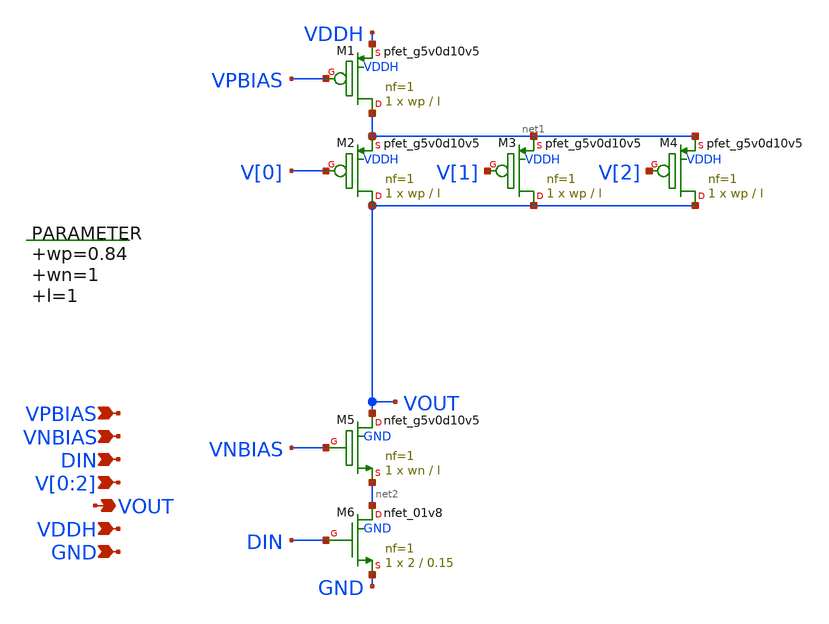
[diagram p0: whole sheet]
** sch_path: xschem/pd_network_parallel.sch
**.subckt pd_network_parallel VPBIAS VNBIAS DIN V[0],V[1],V[2] VOUT VDDH GND
*.ipin VPBIAS
*.ipin VNBIAS
*.ipin DIN
*.ipin V[0],V[1],V[2]
*.opin VOUT
*.ipin VDDH
*.ipin GND
.param wp=0.84 wn=1 l=1

XM1 net1 VPBIAS VDDH VDDH sky130_fd_pr__pfet_g5v0d10v5 L=l W=wp nf=1 ad='int((nf+1)/2) * W/nf * 0.29'
+ as='int((nf+2)/2) * W/nf * 0.29' pd='2*int((nf+1)/2) * (W/nf + 0.29)' ps='2*int((nf+2)/2) * (W/nf + 0.29)'
+ nrd='0.29 / W' nrs='0.29 / W' sa=0 sb=0 sd=0 mult=1 m=1
XM5 VOUT VNBIAS net2 GND sky130_fd_pr__nfet_g5v0d10v5 L=l W=wn nf=1 ad='int((nf+1)/2) * W/nf * 0.29'
+ as='int((nf+2)/2) * W/nf * 0.29' pd='2*int((nf+1)/2) * (W/nf + 0.29)' ps='2*int((nf+2)/2) * (W/nf + 0.29)'
+ nrd='0.29 / W' nrs='0.29 / W' sa=0 sb=0 sd=0 mult=1 m=1
XM2 VOUT V[0] net1 VDDH sky130_fd_pr__pfet_g5v0d10v5 L=l W=wp nf=1 ad='int((nf+1)/2) * W/nf * 0.29' as='int((nf+2)/2) * W/nf * 0.29'
+ pd='2*int((nf+1)/2) * (W/nf + 0.29)' ps='2*int((nf+2)/2) * (W/nf + 0.29)' nrd='0.29 / W' nrs='0.29 / W'
+ sa=0 sb=0 sd=0 mult=1 m=1
XM3 VOUT V[1] net1 VDDH sky130_fd_pr__pfet_g5v0d10v5 L=l W=wp nf=1 ad='int((nf+1)/2) * W/nf * 0.29' as='int((nf+2)/2) * W/nf * 0.29'
+ pd='2*int((nf+1)/2) * (W/nf + 0.29)' ps='2*int((nf+2)/2) * (W/nf + 0.29)' nrd='0.29 / W' nrs='0.29 / W'
+ sa=0 sb=0 sd=0 mult=1 m=1
XM4 VOUT V[2] net1 VDDH sky130_fd_pr__pfet_g5v0d10v5 L=l W=wp nf=1 ad='int((nf+1)/2) * W/nf * 0.29' as='int((nf+2)/2) * W/nf * 0.29'
+ pd='2*int((nf+1)/2) * (W/nf + 0.29)' ps='2*int((nf+2)/2) * (W/nf + 0.29)' nrd='0.29 / W' nrs='0.29 / W'
+ sa=0 sb=0 sd=0 mult=1 m=1
XM6 net2 DIN GND GND sky130_fd_pr__nfet_01v8 L=0.15 W=2 nf=1 ad='int((nf+1)/2) * W/nf * 0.29' as='int((nf+2)/2) * W/nf * 0.29'
+ pd='2*int((nf+1)/2) * (W/nf + 0.29)' ps='2*int((nf+2)/2) * (W/nf + 0.29)' nrd='0.29 / W' nrs='0.29 / W'
+ sa=0 sb=0 sd=0 mult=1 m=1
**.ends
.end
